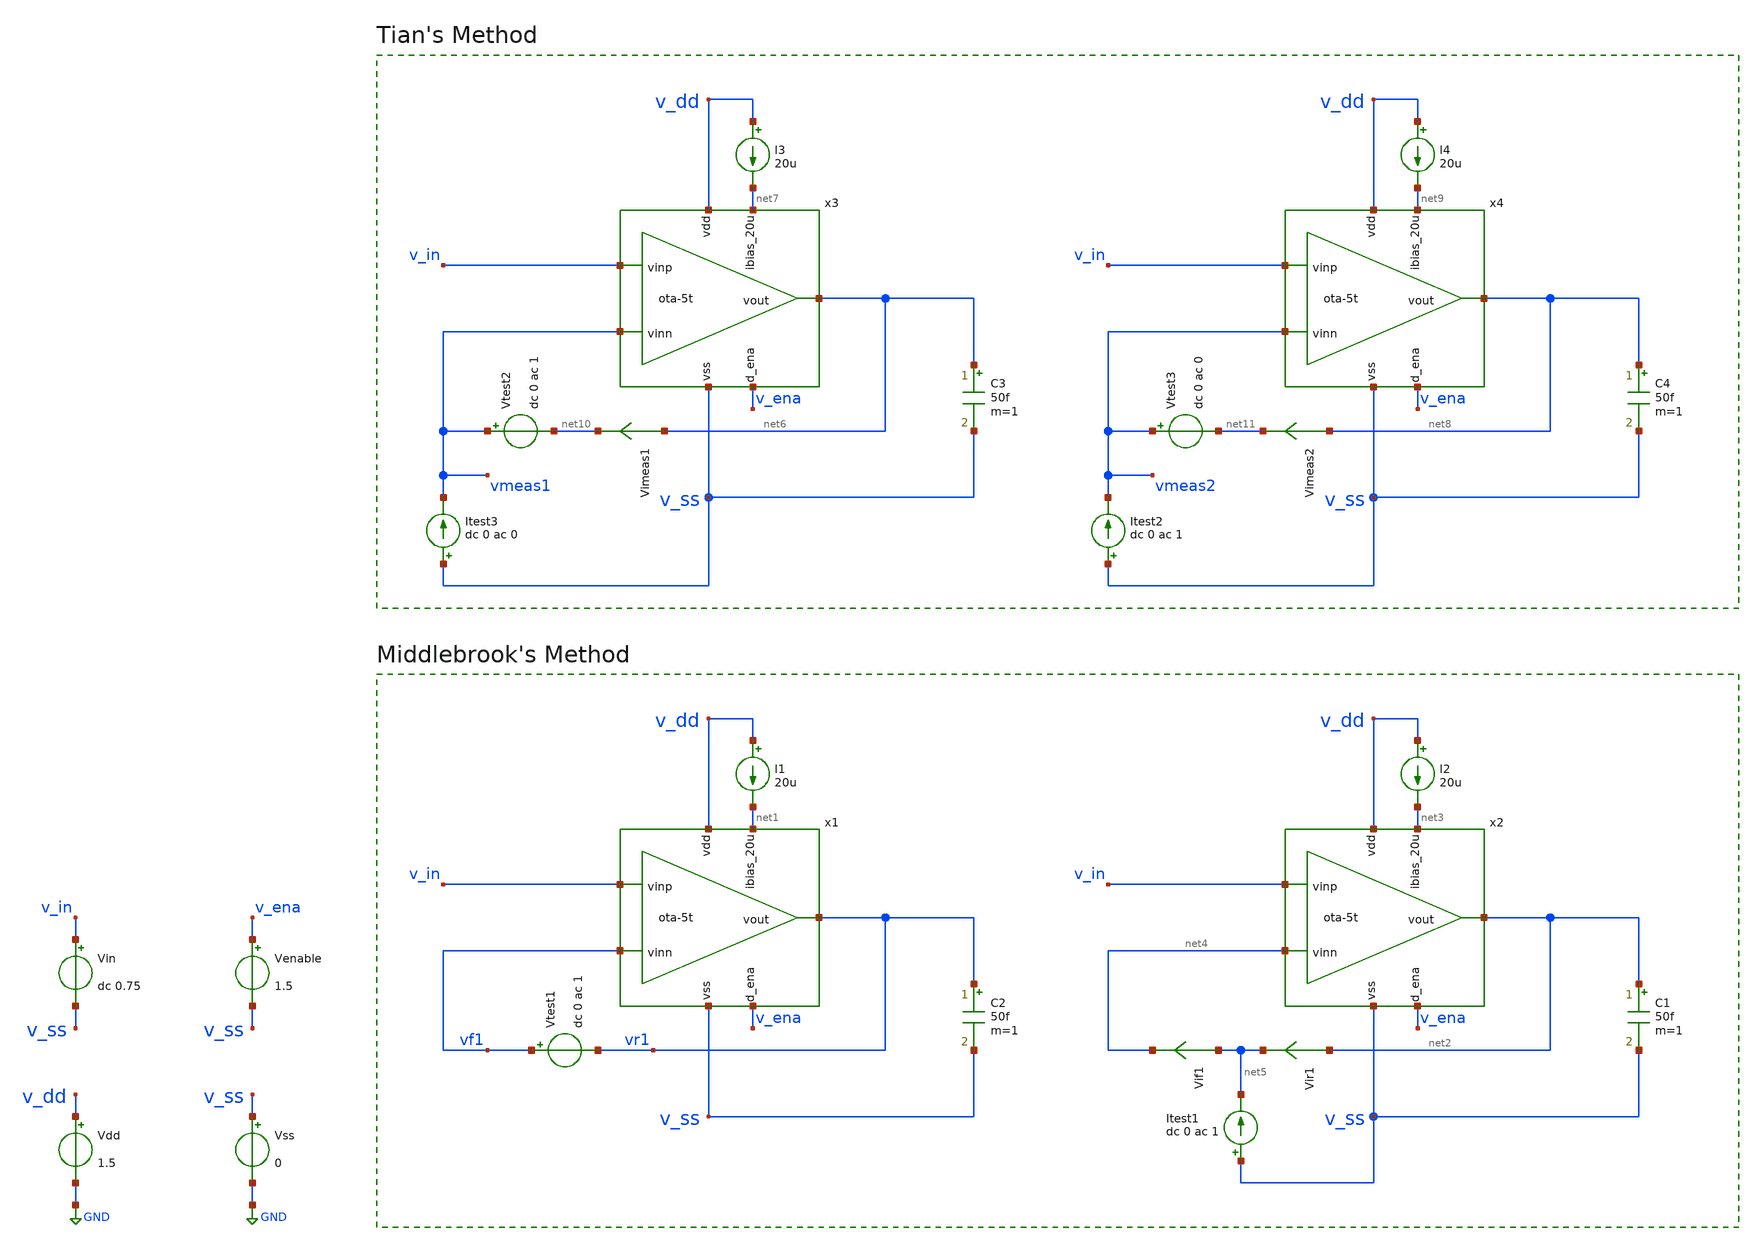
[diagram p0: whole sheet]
** sch_path: platform/examples/OTA/5t-ota/ihp-sg13g2/xschem/ota-5t_tb-loopgain.sch
* (c) 2024 H. Pretl, S. Dorrer, Apache-2.0 license
* platform/examples/OTA/5t-ota/ihp-sg13g2/xschem/ota-5t.sch:
* (c) 2024-2025 H. Pretl, Apache-2.0 license
**.subckt ota-5t_tb-loopgain
Vdd v_dd GND 1.5
Vss v_ss GND 0
Vin v_in v_ss dc 0.75
Venable v_ena v_ss 1.5
C2 vr1 v_ss 50f m=1
I1 v_dd net1 20u
x1 v_dd vr1 v_in vf1 net1 v_ena v_ss ota-5t
Vtest1 vf1 vr1 dc 0 ac 1
C1 net2 v_ss 50f m=1
I2 v_dd net3 20u
x2 v_dd net2 v_in net4 net3 v_ena v_ss ota-5t
Vir1 net2 net5 0
Vif1 net5 net4 0
Itest1 v_ss net5 dc 0 ac 1
C3 net6 v_ss 50f m=1
I3 v_dd net7 20u
x3 v_dd net6 v_in vmeas1 net7 v_ena v_ss ota-5t
C4 net8 v_ss 50f m=1
I4 v_dd net9 20u
x4 v_dd net8 v_in vmeas2 net9 v_ena v_ss ota-5t
Itest3 v_ss vmeas1 dc 0 ac 0
Vtest2 vmeas1 net10 dc 0 ac 1
Vimeas1 net6 net10 0
Itest2 v_ss vmeas2 dc 0 ac 1
Vtest3 vmeas2 net11 dc 0 ac 0
Vimeas2 net8 net11 0
**** begin user architecture code
 .lib cornerMOSlv.lib mos_tt




.param temp=27
.options savecurrents
.options reltol=1e-3 abstol=1e-12 gmin=1e-15

.control

    echo ==================================
    echo start of Control
    echo ==================================

    save all

    echo
    echo (A) start of OP
    echo ----------------------------------

    * Operating Point Analysis (not needed in the optimization... could be turned on but it is
+ turned off to save sim time)
    op
    remzerovec
    write
    set appendwrite

    echo
    echo (B) start of AC Sim
    echo ----------------------------------

    * save the vectors needed in the post-processing (optional - to improve speed... should not use 'save all')
    save vr1 vf1 vir1 vif1 vmeas2 Vimeas2 vmeas1 Vimeas1

    * AC Analysis
    ac dec 101 1 100G

    echo (1) performing Middlebrook's Method

    * Middlebrook's Method
    let tv=-v(vr1)/v(vf1)
    let ti=-i(vir1)/i(vif1)
    let tmb=(tv*ti - 1)/(tv + ti + 2)

    *plot db(tmb) ylabel 'Magnitude - Middlebrook'
    *plot 180/pi*cphase(tmb) ylabel 'Phase - Middlebrook'

    echo (2) performing Tian's Method

    * Tian's Method
    * vtest=0, itest=1:
    let A=i(Vimeas2)
    let C=v(vmeas2)

    * vtest=1, itest=0:
    let B=i(Vimeas1)
    let D=v(vmeas1)
    let ttian=(A*D-B*C-A)/(2*(B*C-A*D)+A-D+1)

    *plot db(ttian) ylabel 'Magnitude - Tian'
    *plot 180/pi*cphase(ttian) ylabel 'Phase - Tian'


    echo (3) measuring performance metrics

    * magnitude
    let out = tmb
    let out_mag = db(out)
    let out_phase = cphase(tmb) * 180/pi

    meas ac GMAX max out_mag

    meas ac DCGAIN MAX out_mag FROM=10 TO=10k

    let f3db = DCGAIN-3
    meas ac FBW WHEN out_mag=f3db FALL=1

    meas ac unity_gain_phase find out_phase when out_mag=0
    meas ac UGF when out_mag=0 fall=1

    let PM = (180-unity_gain_phase) % 180
    print DCGAIN FBW PM UGF

    * Output measured metrics to a file (optional)
    * print DCGAIN FBW PM UGF > meas_results.txt

    echo (4) plotting...

    * Middlebrook vs. Tian
    plot db(tmb) db(ttian) ylabel 'Magnitude'
    plot 180/pi*cphase(tmb) 180/pi*cphase(ttian) ylabel 'Phase'

    echo ----------------------------------
    echo END of AC sim
    echo  ----------------------------------

    echo SAVING SIMULATION RESULTS IN THE RAW FILE
    * save out DCGAIN PM FBW UGF
    write

    echo ==================================
    echo END of Control
    echo ==================================

    * quit

.endc






.param x_dut_nfet_input_w=0.5u
.param x_dut_nfet_input_l=5.0u

.param x_dut_nfet_mirror_w=2.0u
.param x_dut_nfet_mirror_l=5.0u

.param x_dut_pfet_load_w=1.5u
.param x_dut_pfet_load_l=5.0u



**** end user architecture code
**.ends

* expanding   symbol:  ota-5t.sym # of pins=7
** sym_path: ota-5t.sym
** sch_path: ota-5t.sch
.subckt ota-5t vdd vout vinp vinn ibias_20u d_ena vss
*.ipin ibias_20u
*.iopin vdd
*.iopin vss
*.ipin vinp
*.ipin vinn
*.opin vout
*.ipin d_ena
XM5 tail gate_n vss vss sg13_lv_nmos w=x_dut_nfet_mirror_w l=x_dut_nfet_mirror_l ng=1 m=1 mm_ok=1
XM4 vout gate_p vdd vdd sg13_lv_pmos w=x_dut_pfet_load_w l=x_dut_pfet_load_l ng=1 m=1 mm_ok=1
XM1 gate_p vinp tail vss sg13_lv_nmos w=x_dut_nfet_input_w l=x_dut_nfet_input_l ng=1 m=1 mm_ok=1
XM2 vout vinn tail vss sg13_lv_nmos w=x_dut_nfet_input_w l=x_dut_nfet_input_l ng=1 m=1 mm_ok=1
XM3 gate_p gate_p vdd vdd sg13_lv_pmos w=x_dut_pfet_load_w l=x_dut_pfet_load_l ng=1 m=1 mm_ok=1
XM6 ibias_20u gate_n vss vss sg13_lv_nmos w=x_dut_nfet_mirror_ref_w l=x_dut_nfet_mirror_ref_l ng=1
+ m=1 mm_ok=1
XM9 gate_n ena_n vss vss sg13_lv_nmos w=0.5u l=0.13u ng=1 m=1 mm_ok=1
XM11 gate_p ena vdd vdd sg13_lv_pmos w=1.5u l=0.13u ng=1 m=1 mm_ok=1
XM7 ena ena_n vss vss sg13_lv_nmos w=0.5u l=0.13u ng=1 m=1 mm_ok=1
XM8 ena ena_n vdd vdd sg13_lv_pmos w=1.5u l=0.13u ng=1 m=1 mm_ok=1
XM10 ibias_20u ena gate_n vss sg13_lv_nmos w=0.5u l=0.13u ng=1 m=1 mm_ok=1
XM12 ena_n d_ena vss vss sg13_lv_nmos w=0.5u l=0.13u ng=1 m=1 mm_ok=1
XM13 ena_n d_ena vdd vdd sg13_lv_pmos w=1.5u l=0.13u ng=1 m=1 mm_ok=1
.ends

.GLOBAL GND
.end
